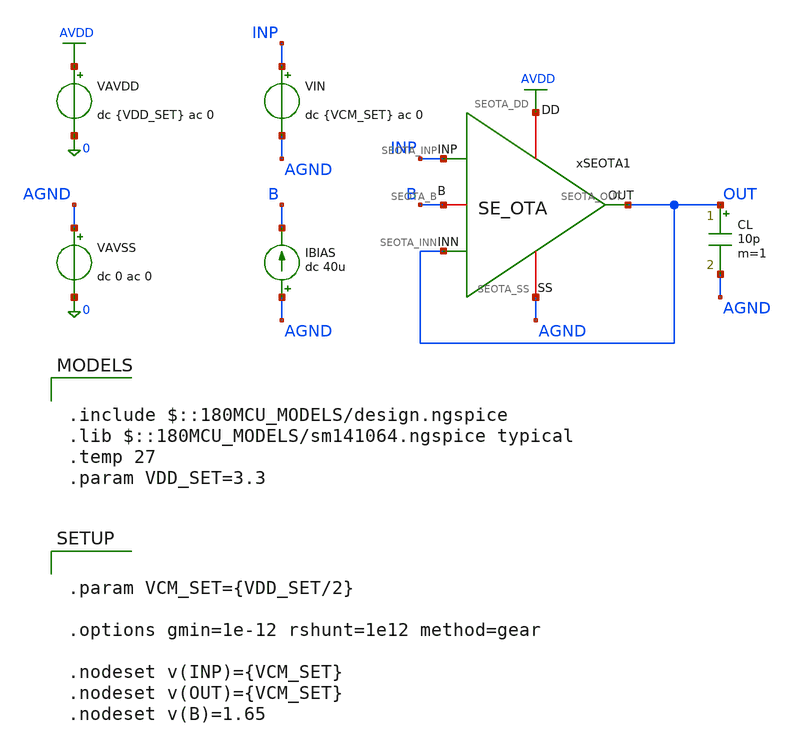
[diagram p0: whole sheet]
** sch_path: Design_Files/IC Design/Testbench/SE_OTA/Close_Loop/SE_OTA_TB_CL_NOM.sch
**.subckt SE_OTA_TB_CL_NOM
CL OUT AGND 10p m=1
xSEOTA1 AVDD AGND INP OUT OUT B SE_OTA
IBIAS AGND B dc 40u
VAVDD AVDD 0 dc {VDD_SET} ac 0
.save i(vavdd)
VIN INP AGND dc {VCM_SET} ac 0
VAVSS AGND 0 dc 0 ac 0
.save i(vavss)
**** begin user architecture code

.include $::180MCU_MODELS/design.ngspice
.lib $::180MCU_MODELS/sm141064.ngspice typical
.temp 27
.param VDD_SET=3.3




.control
destroy all
save all
set wr_vecnames
set wr_singlescale
option numdgt=15

shell mkdir -p
+ /foss/designs/ECG_Acquisition_IC/Measurement_Results/IC_Simulation/SE_OTA/NOM.Result_txt

shell rm -f
+ /foss/designs/ECG_Acquisition_IC/Measurement_Results/IC_Simulation/SE_OTA/NOM.Result_txt/NOM.cl_op.txt
shell rm -f
+ /foss/designs/ECG_Acquisition_IC/Measurement_Results/IC_Simulation/SE_OTA/NOM.Result_txt/NOM.cl_dc.txt
shell rm -f
+ /foss/designs/ECG_Acquisition_IC/Measurement_Results/IC_Simulation/SE_OTA/NOM.Result_txt/NOM.cl_tran.txt

* OP
op

let vdd = v(AVDD)-v(AGND)
let vin = v(INP)-v(AGND)
let vout = v(OUT)-v(AGND)
let vin_diff = v(INP)-v(OUT)
let idd = -vavdd#branch
let ibias = 40u + 0*v(AVDD)

wrdata
+ /foss/designs/ECG_Acquisition_IC/Measurement_Results/IC_Simulation/SE_OTA/NOM.Result_txt/NOM.cl_op.txt vdd vin vout vin_diff v(B) idd ibias

* DC
op
let avdd_run = v(AVDD)-v(AGND)
let vin_low = 0
let vin_high = avdd_run

dc VIN $&vin_low $&vin_high 0.001

let cl_vin = v(INP)-v(AGND)
let cl_vout = v(OUT)-v(AGND)
let cl_err = cl_vout-cl_vin
let cl_vin_diff = v(INP)-v(OUT)
let cl_idd = -vavdd#branch
let cl_ibias = 40u + 0*v(AVDD)
let cl_iout = 10e-12*deriv(cl_vout)

setscale cl_vin

wrdata
+ /foss/designs/ECG_Acquisition_IC/Measurement_Results/IC_Simulation/SE_OTA/NOM.Result_txt/NOM.cl_dc.txt cl_vout cl_err cl_vin_diff cl_idd cl_ibias cl_iout

* Tran
reset
save all
set wr_vecnames
set wr_singlescale
option numdgt=15

alter @VIN[PULSE] = [ 1.0 2.0 1u 10n 10n 10u 20u 0 ]

tran 0.5n 30u

let tr_vin = v(INP)-v(AGND)
let tr_vout = v(OUT)-v(AGND)
let tr_err = tr_vout-tr_vin
let tr_vin_diff = v(INP)-v(OUT)
let tr_idd = -vavdd#branch
let tr_iout = 10e-12*deriv(tr_vout)

setscale time

wrdata
+ /foss/designs/ECG_Acquisition_IC/Measurement_Results/IC_Simulation/SE_OTA/NOM.Result_txt/NOM.cl_tran.txt tr_vin tr_vout tr_err tr_vin_diff tr_idd tr_iout

quit
.endc




.param VCM_SET={VDD_SET/2}

.options gmin=1e-12 rshunt=1e12 method=gear

.nodeset v(INP)={VCM_SET}
.nodeset v(OUT)={VCM_SET}
.nodeset v(B)=1.65


**** end user architecture code
**.ends

* expanding   symbol:  ECG_Acquisition_IC/Design_Files/IC Design/Schematic/SE_OTA/SE_OTA.sym # of
*+ pins=6
** sym_path: Design_Files/IC Design/Schematic/SE_OTA/SE_OTA.sym
** sch_path: Design_Files/IC Design/Schematic/SE_OTA/SE_OTA.sch
.subckt SE_OTA SEOTA_DD SEOTA_SS SEOTA_INP SEOTA_INN SEOTA_OUT SEOTA_B
*.iopin SEOTA_DD
*.iopin SEOTA_SS
*.ipin SEOTA_INP
*.ipin SEOTA_INN
*.opin SEOTA_OUT
*.iopin SEOTA_B
XM3 net4 net4 SEOTA_DD SEOTA_DD pfet_03v3 L=4u W=1u nf=1 ad='int((nf+1)/2) * W/nf * 0.18u' as='int((nf+2)/2) * W/nf * 0.18u'
+ pd='2*int((nf+1)/2) * (W/nf + 0.18u)' ps='2*int((nf+2)/2) * (W/nf + 0.18u)' nrd='0.18u / W' nrs='0.18u / W'
+ sa=0 sb=0 sd=0 m=60
XM7 SEOTA_OUT SEOTA_B SEOTA_SS SEOTA_SS nfet_03v3 L=0.5u W=1u nf=1 ad='int((nf+1)/2) * W/nf * 0.18u'
+ as='int((nf+2)/2) * W/nf * 0.18u' pd='2*int((nf+1)/2) * (W/nf + 0.18u)' ps='2*int((nf+2)/2) * (W/nf + 0.18u)'
+ nrd='0.18u / W' nrs='0.18u / W' sa=0 sb=0 sd=0 m=100
Rz net1 net2 3.8k m=1
XM5 net3 SEOTA_B SEOTA_SS SEOTA_SS nfet_03v3 L=2u W=1u nf=1 ad='int((nf+1)/2) * W/nf * 0.18u' as='int((nf+2)/2) * W/nf * 0.18u'
+ pd='2*int((nf+1)/2) * (W/nf + 0.18u)' ps='2*int((nf+2)/2) * (W/nf + 0.18u)' nrd='0.18u / W' nrs='0.18u / W'
+ sa=0 sb=0 sd=0 m=10
XM6 SEOTA_OUT net1 SEOTA_DD SEOTA_DD pfet_03v3 L=0.5u W=1u nf=1 ad='int((nf+1)/2) * W/nf * 0.18u' as='int((nf+2)/2) * W/nf * 0.18u'
+ pd='2*int((nf+1)/2) * (W/nf + 0.18u)' ps='2*int((nf+2)/2) * (W/nf + 0.18u)' nrd='0.18u / W' nrs='0.18u / W'
+ sa=0 sb=0 sd=0 m=400
XM8 SEOTA_B SEOTA_B SEOTA_SS SEOTA_SS nfet_03v3 L=2u W=1u nf=1 ad='int((nf+1)/2) * W/nf * 0.18u' as='int((nf+2)/2) * W/nf * 0.18u'
+ pd='2*int((nf+1)/2) * (W/nf + 0.18u)' ps='2*int((nf+2)/2) * (W/nf + 0.18u)' nrd='0.18u / W' nrs='0.18u / W'
+ sa=0 sb=0 sd=0 m=20
Cc net2 SEOTA_OUT 2p m=1
XM4 net1 net4 SEOTA_DD SEOTA_DD pfet_03v3 L=4u W=1u nf=1 ad='int((nf+1)/2) * W/nf * 0.18u' as='int((nf+2)/2) * W/nf * 0.18u'
+ pd='2*int((nf+1)/2) * (W/nf + 0.18u)' ps='2*int((nf+2)/2) * (W/nf + 0.18u)' nrd='0.18u / W' nrs='0.18u / W'
+ sa=0 sb=0 sd=0 m=60
XM1 net4 SEOTA_INN net3 SEOTA_SS nfet_03v3 L=4u W=1u nf=1 ad='int((nf+1)/2) * W/nf * 0.18u' as='int((nf+2)/2) * W/nf * 0.18u'
+ pd='2*int((nf+1)/2) * (W/nf + 0.18u)' ps='2*int((nf+2)/2) * (W/nf + 0.18u)' nrd='0.18u / W' nrs='0.18u / W'
+ sa=0 sb=0 sd=0 m=400
XM2 net1 SEOTA_INP net3 SEOTA_SS nfet_03v3 L=4u W=1u nf=1 ad='int((nf+1)/2) * W/nf * 0.18u' as='int((nf+2)/2) * W/nf * 0.18u'
+ pd='2*int((nf+1)/2) * (W/nf + 0.18u)' ps='2*int((nf+2)/2) * (W/nf + 0.18u)' nrd='0.18u / W' nrs='0.18u / W'
+ sa=0 sb=0 sd=0 m=400
.ends

.GLOBAL AVDD
.end
